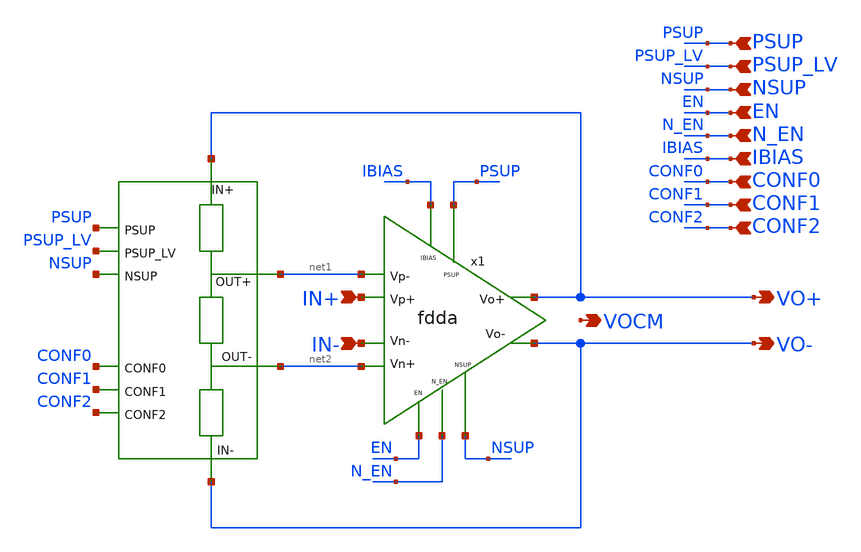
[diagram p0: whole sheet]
** sch_path: xschem/blocks/in_amp/in_amp.sch
**.subckt in_amp VO+ VO- IN+ IN- PSUP NSUP EN N_EN IBIAS PSUP_LV CONF0 CONF1 CONF2 VOCM
*.opin VO+
*.opin VO-
*.ipin IN+
*.ipin IN-
*.ipin PSUP
*.ipin NSUP
*.ipin EN
*.ipin N_EN
*.ipin IBIAS
*.ipin PSUP_LV
*.ipin CONF0
*.ipin CONF1
*.ipin CONF2
*.opin VOCM
x1 PSUP net1 IN- net2 IN+ VO+ VO- IBIAS N_EN EN NSUP fdda
**.ends

* expanding   symbol:  blocks/fdda/fdda.sym # of pins=11
** sym_path: xschem/blocks/fdda/fdda.sym
** sch_path: xschem/blocks/fdda/fdda.sch
.subckt fdda PSUP Vp- Vn+ Vn- Vp+ Vo+ Vo- IBIAS N_EN EN NSUP
*.ipin PSUP
*.ipin NSUP
*.ipin N_EN
*.ipin EN
*.ipin IBIAS
*.ipin Vp+
*.ipin Vp-
*.ipin Vn+
*.ipin Vn-
*.opin Vo+
*.opin Vo-
* noconn N_EN
* noconn EN
I0 net5 NSUP 1u
XM9 Vo+ Vp- net1 NSUP pfet_06v0 L=2u W=4u nf=5 ad='int((nf+1)/2) * W/nf * 0.18u' as='int((nf+2)/2) * W/nf * 0.18u'
+ pd='2*int((nf+1)/2) * (W/nf + 0.18u)' ps='2*int((nf+2)/2) * (W/nf + 0.18u)' nrd='0.18u / W' nrs='0.18u / W'
+ sa=0 sb=0 sd=0 m=10
XM1 Vo- Vp+ net1 NSUP pfet_06v0 L=2u W=4u nf=5 ad='int((nf+1)/2) * W/nf * 0.18u' as='int((nf+2)/2) * W/nf * 0.18u'
+ pd='2*int((nf+1)/2) * (W/nf + 0.18u)' ps='2*int((nf+2)/2) * (W/nf + 0.18u)' nrd='0.18u / W' nrs='0.18u / W'
+ sa=0 sb=0 sd=0 m=10
XM2 net1 vb1 PSUP net3 pfet_06v0 L=4u W=2u nf=1 ad='int((nf+1)/2) * W/nf * 0.18u' as='int((nf+2)/2) * W/nf * 0.18u'
+ pd='2*int((nf+1)/2) * (W/nf + 0.18u)' ps='2*int((nf+2)/2) * (W/nf + 0.18u)' nrd='0.18u / W' nrs='0.18u / W'
+ sa=0 sb=0 sd=0 m=8
XM3 Vo- Vo- NSUP NSUP nfet_06v0 L=4u W=2u nf=1 ad='int((nf+1)/2) * W/nf * 0.18u' as='int((nf+2)/2) * W/nf * 0.18u'
+ pd='2*int((nf+1)/2) * (W/nf + 0.18u)' ps='2*int((nf+2)/2) * (W/nf + 0.18u)' nrd='0.18u / W' nrs='0.18u / W'
+ sa=0 sb=0 sd=0 m=4
XM4 Vo+ Vn- net2 NSUP pfet_06v0 L=2u W=4u nf=5 ad='int((nf+1)/2) * W/nf * 0.18u' as='int((nf+2)/2) * W/nf * 0.18u'
+ pd='2*int((nf+1)/2) * (W/nf + 0.18u)' ps='2*int((nf+2)/2) * (W/nf + 0.18u)' nrd='0.18u / W' nrs='0.18u / W'
+ sa=0 sb=0 sd=0 m=10
XM5 Vo- Vn+ net2 NSUP pfet_06v0 L=2u W=4u nf=5 ad='int((nf+1)/2) * W/nf * 0.18u' as='int((nf+2)/2) * W/nf * 0.18u'
+ pd='2*int((nf+1)/2) * (W/nf + 0.18u)' ps='2*int((nf+2)/2) * (W/nf + 0.18u)' nrd='0.18u / W' nrs='0.18u / W'
+ sa=0 sb=0 sd=0 m=10
XM6 net2 vb1 PSUP PSUP pfet_06v0 L=4u W=2u nf=1 ad='int((nf+1)/2) * W/nf * 0.18u' as='int((nf+2)/2) * W/nf * 0.18u'
+ pd='2*int((nf+1)/2) * (W/nf + 0.18u)' ps='2*int((nf+2)/2) * (W/nf + 0.18u)' nrd='0.18u / W' nrs='0.18u / W'
+ sa=0 sb=0 sd=0 m=8
XM8 Vo+ Vo+ NSUP NSUP nfet_06v0 L=4u W=2u nf=1 ad='int((nf+1)/2) * W/nf * 0.18u' as='int((nf+2)/2) * W/nf * 0.18u'
+ pd='2*int((nf+1)/2) * (W/nf + 0.18u)' ps='2*int((nf+2)/2) * (W/nf + 0.18u)' nrd='0.18u / W' nrs='0.18u / W'
+ sa=0 sb=0 sd=0 m=4
XM7 net5 vb1 PSUP net4 pfet_06v0 L=4u W=2u nf=1 ad='int((nf+1)/2) * W/nf * 0.18u' as='int((nf+2)/2) * W/nf * 0.18u'
+ pd='2*int((nf+1)/2) * (W/nf + 0.18u)' ps='2*int((nf+2)/2) * (W/nf + 0.18u)' nrd='0.18u / W' nrs='0.18u / W'
+ sa=0 sb=0 sd=0 m=4
.ends

.end
